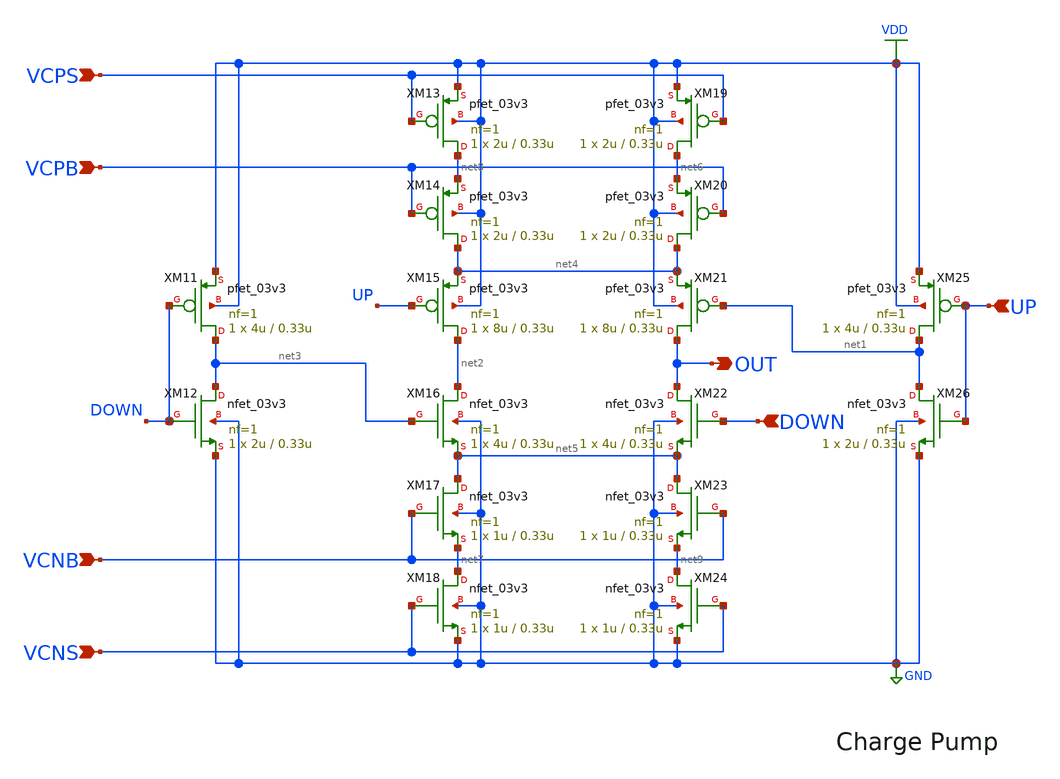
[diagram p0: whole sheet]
** sch_path: 1st_Design/cp.sch
**.subckt cp DOWN UP OUT VCPS VCPB VCNB VCNS
*.ipin DOWN
*.ipin UP
*.opin OUT
*.ipin VCPS
*.ipin VCPB
*.ipin VCNB
*.ipin VCNS
XM15 net2 UP net4 VDD pfet_03v3 L=0.33u W=8u nf=1 ad='int((nf+1)/2) * W/nf * 0.18u' as='int((nf+2)/2) * W/nf * 0.18u'
+ pd='2*int((nf+1)/2) * (W/nf + 0.18u)' ps='2*int((nf+2)/2) * (W/nf + 0.18u)' nrd='0.18u / W' nrs='0.18u / W'
+ sa=0 sb=0 sd=0 m=1
XM16 net2 net3 net5 GND nfet_03v3 L=0.33u W=4u nf=1 ad='int((nf+1)/2) * W/nf * 0.18u' as='int((nf+2)/2) * W/nf * 0.18u'
+ pd='2*int((nf+1)/2) * (W/nf + 0.18u)' ps='2*int((nf+2)/2) * (W/nf + 0.18u)' nrd='0.18u / W' nrs='0.18u / W'
+ sa=0 sb=0 sd=0 m=1
XM11 net3 DOWN VDD VDD pfet_03v3 L=0.33u W=4u nf=1 ad='int((nf+1)/2) * W/nf * 0.18u' as='int((nf+2)/2) * W/nf * 0.18u'
+ pd='2*int((nf+1)/2) * (W/nf + 0.18u)' ps='2*int((nf+2)/2) * (W/nf + 0.18u)' nrd='0.18u / W' nrs='0.18u / W'
+ sa=0 sb=0 sd=0 m=1
XM12 net3 DOWN GND GND nfet_03v3 L=0.33u W=2u nf=1 ad='int((nf+1)/2) * W/nf * 0.18u' as='int((nf+2)/2) * W/nf * 0.18u'
+ pd='2*int((nf+1)/2) * (W/nf + 0.18u)' ps='2*int((nf+2)/2) * (W/nf + 0.18u)' nrd='0.18u / W' nrs='0.18u / W'
+ sa=0 sb=0 sd=0 m=1
XM17 net5 VCNB net7 GND nfet_03v3 L=0.33u W=1u nf=1 ad='int((nf+1)/2) * W/nf * 0.18u' as='int((nf+2)/2) * W/nf * 0.18u'
+ pd='2*int((nf+1)/2) * (W/nf + 0.18u)' ps='2*int((nf+2)/2) * (W/nf + 0.18u)' nrd='0.18u / W' nrs='0.18u / W'
+ sa=0 sb=0 sd=0 m=1
XM18 net7 VCNS GND GND nfet_03v3 L=0.33u W=1u nf=1 ad='int((nf+1)/2) * W/nf * 0.18u' as='int((nf+2)/2) * W/nf * 0.18u'
+ pd='2*int((nf+1)/2) * (W/nf + 0.18u)' ps='2*int((nf+2)/2) * (W/nf + 0.18u)' nrd='0.18u / W' nrs='0.18u / W'
+ sa=0 sb=0 sd=0 m=1
XM13 net8 VCPS VDD VDD pfet_03v3 L=0.33u W=2u nf=1 ad='int((nf+1)/2) * W/nf * 0.18u' as='int((nf+2)/2) * W/nf * 0.18u'
+ pd='2*int((nf+1)/2) * (W/nf + 0.18u)' ps='2*int((nf+2)/2) * (W/nf + 0.18u)' nrd='0.18u / W' nrs='0.18u / W'
+ sa=0 sb=0 sd=0 m=1
XM14 net4 VCPB net8 VDD pfet_03v3 L=0.33u W=2u nf=1 ad='int((nf+1)/2) * W/nf * 0.18u' as='int((nf+2)/2) * W/nf * 0.18u'
+ pd='2*int((nf+1)/2) * (W/nf + 0.18u)' ps='2*int((nf+2)/2) * (W/nf + 0.18u)' nrd='0.18u / W' nrs='0.18u / W'
+ sa=0 sb=0 sd=0 m=1
XM19 net6 VCPS VDD VDD pfet_03v3 L=0.33u W=2u nf=1 ad='int((nf+1)/2) * W/nf * 0.18u' as='int((nf+2)/2) * W/nf * 0.18u'
+ pd='2*int((nf+1)/2) * (W/nf + 0.18u)' ps='2*int((nf+2)/2) * (W/nf + 0.18u)' nrd='0.18u / W' nrs='0.18u / W'
+ sa=0 sb=0 sd=0 m=1
XM20 net4 VCPB net6 VDD pfet_03v3 L=0.33u W=2u nf=1 ad='int((nf+1)/2) * W/nf * 0.18u' as='int((nf+2)/2) * W/nf * 0.18u'
+ pd='2*int((nf+1)/2) * (W/nf + 0.18u)' ps='2*int((nf+2)/2) * (W/nf + 0.18u)' nrd='0.18u / W' nrs='0.18u / W'
+ sa=0 sb=0 sd=0 m=1
XM21 OUT net1 net4 VDD pfet_03v3 L=0.33u W=8u nf=1 ad='int((nf+1)/2) * W/nf * 0.18u' as='int((nf+2)/2) * W/nf * 0.18u'
+ pd='2*int((nf+1)/2) * (W/nf + 0.18u)' ps='2*int((nf+2)/2) * (W/nf + 0.18u)' nrd='0.18u / W' nrs='0.18u / W'
+ sa=0 sb=0 sd=0 m=1
XM22 OUT DOWN net5 GND nfet_03v3 L=0.33u W=4u nf=1 ad='int((nf+1)/2) * W/nf * 0.18u' as='int((nf+2)/2) * W/nf * 0.18u'
+ pd='2*int((nf+1)/2) * (W/nf + 0.18u)' ps='2*int((nf+2)/2) * (W/nf + 0.18u)' nrd='0.18u / W' nrs='0.18u / W'
+ sa=0 sb=0 sd=0 m=1
XM23 net5 VCNB net9 GND nfet_03v3 L=0.33u W=1u nf=1 ad='int((nf+1)/2) * W/nf * 0.18u' as='int((nf+2)/2) * W/nf * 0.18u'
+ pd='2*int((nf+1)/2) * (W/nf + 0.18u)' ps='2*int((nf+2)/2) * (W/nf + 0.18u)' nrd='0.18u / W' nrs='0.18u / W'
+ sa=0 sb=0 sd=0 m=1
XM24 net9 VCNS GND GND nfet_03v3 L=0.33u W=1u nf=1 ad='int((nf+1)/2) * W/nf * 0.18u' as='int((nf+2)/2) * W/nf * 0.18u'
+ pd='2*int((nf+1)/2) * (W/nf + 0.18u)' ps='2*int((nf+2)/2) * (W/nf + 0.18u)' nrd='0.18u / W' nrs='0.18u / W'
+ sa=0 sb=0 sd=0 m=1
XM25 net1 UP VDD VDD pfet_03v3 L=0.33u W=4u nf=1 ad='int((nf+1)/2) * W/nf * 0.18u' as='int((nf+2)/2) * W/nf * 0.18u'
+ pd='2*int((nf+1)/2) * (W/nf + 0.18u)' ps='2*int((nf+2)/2) * (W/nf + 0.18u)' nrd='0.18u / W' nrs='0.18u / W'
+ sa=0 sb=0 sd=0 m=1
XM26 net1 UP GND GND nfet_03v3 L=0.33u W=2u nf=1 ad='int((nf+1)/2) * W/nf * 0.18u' as='int((nf+2)/2) * W/nf * 0.18u'
+ pd='2*int((nf+1)/2) * (W/nf + 0.18u)' ps='2*int((nf+2)/2) * (W/nf + 0.18u)' nrd='0.18u / W' nrs='0.18u / W'
+ sa=0 sb=0 sd=0 m=1
**.ends
.GLOBAL VDD
.GLOBAL GND
.end
